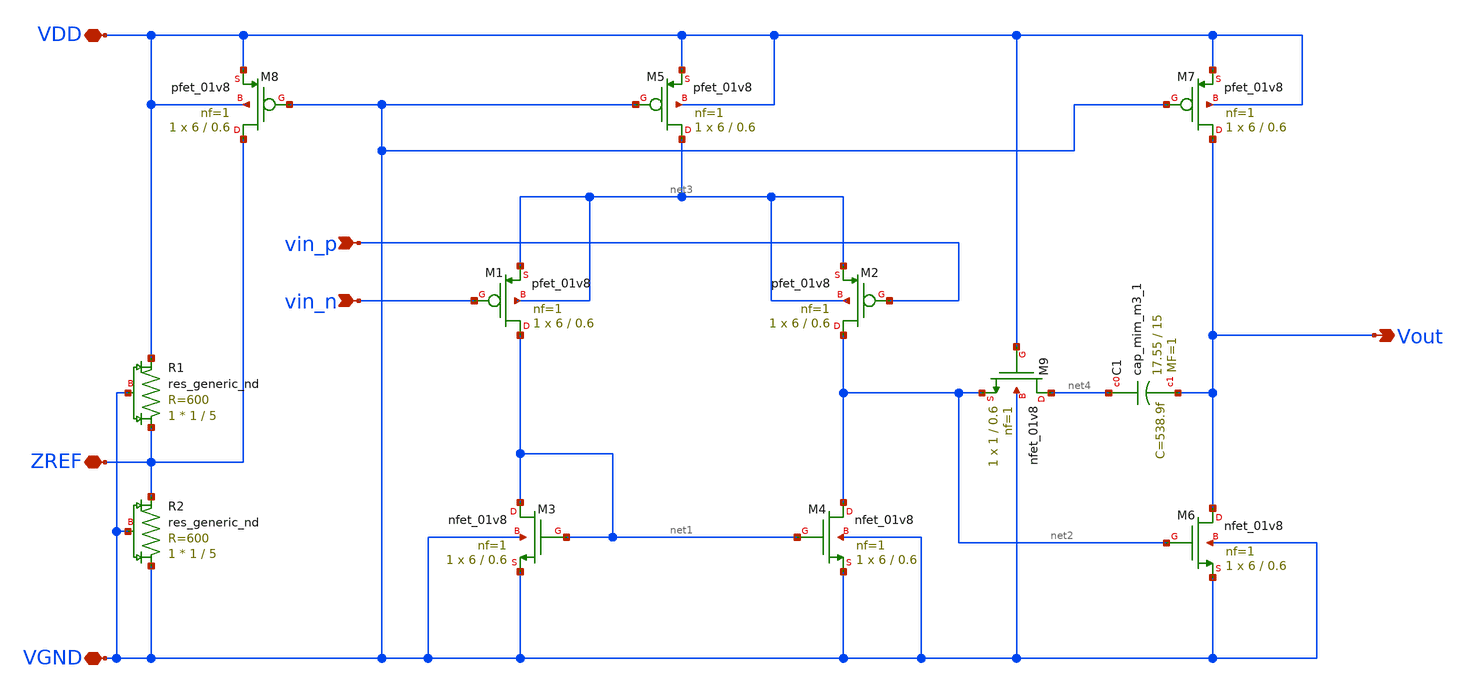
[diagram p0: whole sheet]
** sch_path: xschem/opamp.sch
**.subckt opamp vin_n vin_p Vout VDD ZREF VGND
*.ipin vin_n
*.ipin vin_p
*.opin Vout
*.iopin VDD
*.iopin ZREF
*.iopin VGND
XM1 net1 vin_n net3 net3 sky130_fd_pr__pfet_01v8 L=0.6 W=6 nf=1 ad='W * 0.29' as='W * 0.29' pd='2 * (W + 0.29)'
+ ps='2 * (W + 0.29)' nrd='0.29 / W' nrs='0.29 / W' sa=0 sb=0 sd=0 mult=1 m=1
XM2 net2 vin_p net3 net3 sky130_fd_pr__pfet_01v8 L=0.6 W=6 nf=1 ad='W * 0.29' as='W * 0.29' pd='2 * (W + 0.29)'
+ ps='2 * (W + 0.29)' nrd='0.29 / W' nrs='0.29 / W' sa=0 sb=0 sd=0 mult=1 m=1
XM3 net1 net1 VGND VGND sky130_fd_pr__nfet_01v8 L=0.6 W=6 nf=1 ad='W * 0.29' as='W * 0.29' pd='2 * (W + 0.29)'
+ ps='2 * (W + 0.29)' nrd='0.29 / W' nrs='0.29 / W' sa=0 sb=0 sd=0 mult=1 m=1
XM4 net2 net1 VGND VGND sky130_fd_pr__nfet_01v8 L=0.6 W=6 nf=1 ad='W * 0.29' as='W * 0.29' pd='2 * (W + 0.29)'
+ ps='2 * (W + 0.29)' nrd='0.29 / W' nrs='0.29 / W' sa=0 sb=0 sd=0 mult=1 m=1
XM5 net3 VGND VDD VDD sky130_fd_pr__pfet_01v8 L=0.6 W=6 nf=1 ad='W * 0.29' as='W * 0.29' pd='2 * (W + 0.29)'
+ ps='2 * (W + 0.29)' nrd='0.29 / W' nrs='0.29 / W' sa=0 sb=0 sd=0 mult=1 m=1
XM7 Vout VGND VDD VDD sky130_fd_pr__pfet_01v8 L=0.6 W=6 nf=1 ad='W * 0.29' as='W * 0.29' pd='2 * (W + 0.29)'
+ ps='2 * (W + 0.29)' nrd='0.29 / W' nrs='0.29 / W' sa=0 sb=0 sd=0 mult=1 m=1
XM8 ZREF VGND VDD VDD sky130_fd_pr__pfet_01v8 L=0.6 W=6 nf=1 ad='W * 0.29' as='W * 0.29' pd='2 * (W + 0.29)'
+ ps='2 * (W + 0.29)' nrd='0.29 / W' nrs='0.29 / W' sa=0 sb=0 sd=0 mult=1 m=1
XM9 net4 VDD net2 VGND sky130_fd_pr__nfet_01v8 L=0.6 W=1 nf=1 ad='W * 0.29' as='W * 0.29' pd='2 * (W + 0.29)'
+ ps='2 * (W + 0.29)' nrd='0.29 / W' nrs='0.29 / W' sa=0 sb=0 sd=0 mult=1 m=1
XC1 net4 Vout sky130_fd_pr__cap_mim_m3_1 W=17.55 L=15 MF=1 m=1
XM6 Vout net2 VGND VGND sky130_fd_pr__nfet_01v8 L=0.6 W=6 nf=1 ad='W * 0.29' as='W * 0.29' pd='2 * (W + 0.29)'
+ ps='2 * (W + 0.29)' nrd='0.29 / W' nrs='0.29 / W' sa=0 sb=0 sd=0 mult=1 m=1
XR1 ZREF VDD VGND sky130_fd_pr__res_generic_nd W=1 L=5 mult=1 m=1
XR2 VGND ZREF VGND sky130_fd_pr__res_generic_nd W=1 L=5 mult=1 m=1
**.ends
.end
